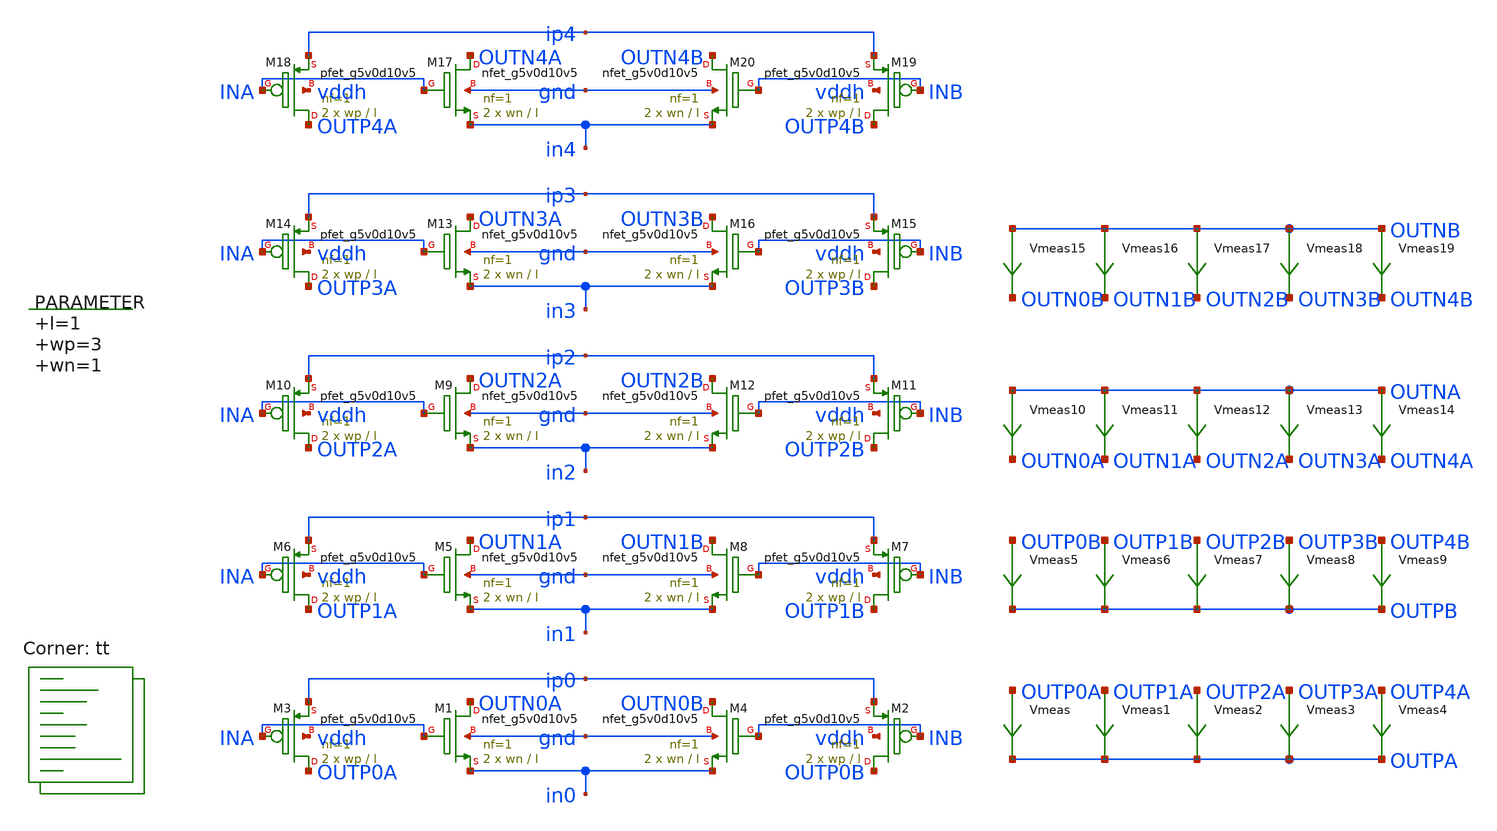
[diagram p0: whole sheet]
** sch_path: xschem/untitled.sch
**.subckt untitled
XM1 OUTN0A INA in0 gnd sky130_fd_pr__nfet_g5v0d10v5 L=l W=wn nf=1 ad='int((nf+1)/2) * W/nf * 0.29' as='int((nf+2)/2) * W/nf * 0.29'
+ pd='2*int((nf+1)/2) * (W/nf + 0.29)' ps='2*int((nf+2)/2) * (W/nf + 0.29)' nrd='0.29 / W' nrs='0.29 / W'
+ sa=0 sb=0 sd=0 mult=2 m=2
XM3 OUTP0A INA ip0 vddh sky130_fd_pr__pfet_g5v0d10v5 L=l W=wp nf=1 ad='int((nf+1)/2) * W/nf * 0.29' as='int((nf+2)/2) * W/nf * 0.29'
+ pd='2*int((nf+1)/2) * (W/nf + 0.29)' ps='2*int((nf+2)/2) * (W/nf + 0.29)' nrd='0.29 / W' nrs='0.29 / W'
+ sa=0 sb=0 sd=0 mult=2 m=2
XM2 OUTP0B INB ip0 vddh sky130_fd_pr__pfet_g5v0d10v5 L=l W=wp nf=1 ad='int((nf+1)/2) * W/nf * 0.29' as='int((nf+2)/2) * W/nf * 0.29'
+ pd='2*int((nf+1)/2) * (W/nf + 0.29)' ps='2*int((nf+2)/2) * (W/nf + 0.29)' nrd='0.29 / W' nrs='0.29 / W'
+ sa=0 sb=0 sd=0 mult=2 m=2
XM4 OUTN0B INB in0 gnd sky130_fd_pr__nfet_g5v0d10v5 L=l W=wn nf=1 ad='int((nf+1)/2) * W/nf * 0.29' as='int((nf+2)/2) * W/nf * 0.29'
+ pd='2*int((nf+1)/2) * (W/nf + 0.29)' ps='2*int((nf+2)/2) * (W/nf + 0.29)' nrd='0.29 / W' nrs='0.29 / W'
+ sa=0 sb=0 sd=0 mult=2 m=2
XM5 OUTN1A INA in1 gnd sky130_fd_pr__nfet_g5v0d10v5 L=l W=wn nf=1 ad='int((nf+1)/2) * W/nf * 0.29' as='int((nf+2)/2) * W/nf * 0.29'
+ pd='2*int((nf+1)/2) * (W/nf + 0.29)' ps='2*int((nf+2)/2) * (W/nf + 0.29)' nrd='0.29 / W' nrs='0.29 / W'
+ sa=0 sb=0 sd=0 mult=2 m=2
XM6 OUTP1A INA ip1 vddh sky130_fd_pr__pfet_g5v0d10v5 L=l W=wp nf=1 ad='int((nf+1)/2) * W/nf * 0.29' as='int((nf+2)/2) * W/nf * 0.29'
+ pd='2*int((nf+1)/2) * (W/nf + 0.29)' ps='2*int((nf+2)/2) * (W/nf + 0.29)' nrd='0.29 / W' nrs='0.29 / W'
+ sa=0 sb=0 sd=0 mult=2 m=2
XM7 OUTP1B INB ip1 vddh sky130_fd_pr__pfet_g5v0d10v5 L=l W=wp nf=1 ad='int((nf+1)/2) * W/nf * 0.29' as='int((nf+2)/2) * W/nf * 0.29'
+ pd='2*int((nf+1)/2) * (W/nf + 0.29)' ps='2*int((nf+2)/2) * (W/nf + 0.29)' nrd='0.29 / W' nrs='0.29 / W'
+ sa=0 sb=0 sd=0 mult=2 m=2
XM8 OUTN1B INB in1 gnd sky130_fd_pr__nfet_g5v0d10v5 L=l W=wn nf=1 ad='int((nf+1)/2) * W/nf * 0.29' as='int((nf+2)/2) * W/nf * 0.29'
+ pd='2*int((nf+1)/2) * (W/nf + 0.29)' ps='2*int((nf+2)/2) * (W/nf + 0.29)' nrd='0.29 / W' nrs='0.29 / W'
+ sa=0 sb=0 sd=0 mult=2 m=2
XM9 OUTN2A INA in2 gnd sky130_fd_pr__nfet_g5v0d10v5 L=l W=wn nf=1 ad='int((nf+1)/2) * W/nf * 0.29' as='int((nf+2)/2) * W/nf * 0.29'
+ pd='2*int((nf+1)/2) * (W/nf + 0.29)' ps='2*int((nf+2)/2) * (W/nf + 0.29)' nrd='0.29 / W' nrs='0.29 / W'
+ sa=0 sb=0 sd=0 mult=2 m=2
XM10 OUTP2A INA ip2 vddh sky130_fd_pr__pfet_g5v0d10v5 L=l W=wp nf=1 ad='int((nf+1)/2) * W/nf * 0.29'
+ as='int((nf+2)/2) * W/nf * 0.29' pd='2*int((nf+1)/2) * (W/nf + 0.29)' ps='2*int((nf+2)/2) * (W/nf + 0.29)'
+ nrd='0.29 / W' nrs='0.29 / W' sa=0 sb=0 sd=0 mult=2 m=2
XM11 OUTP2B INB ip2 vddh sky130_fd_pr__pfet_g5v0d10v5 L=l W=wp nf=1 ad='int((nf+1)/2) * W/nf * 0.29'
+ as='int((nf+2)/2) * W/nf * 0.29' pd='2*int((nf+1)/2) * (W/nf + 0.29)' ps='2*int((nf+2)/2) * (W/nf + 0.29)'
+ nrd='0.29 / W' nrs='0.29 / W' sa=0 sb=0 sd=0 mult=2 m=2
XM12 OUTN2B INB in2 gnd sky130_fd_pr__nfet_g5v0d10v5 L=l W=wn nf=1 ad='int((nf+1)/2) * W/nf * 0.29' as='int((nf+2)/2) * W/nf * 0.29'
+ pd='2*int((nf+1)/2) * (W/nf + 0.29)' ps='2*int((nf+2)/2) * (W/nf + 0.29)' nrd='0.29 / W' nrs='0.29 / W'
+ sa=0 sb=0 sd=0 mult=2 m=2
XM13 OUTN3A INA in3 gnd sky130_fd_pr__nfet_g5v0d10v5 L=l W=wn nf=1 ad='int((nf+1)/2) * W/nf * 0.29' as='int((nf+2)/2) * W/nf * 0.29'
+ pd='2*int((nf+1)/2) * (W/nf + 0.29)' ps='2*int((nf+2)/2) * (W/nf + 0.29)' nrd='0.29 / W' nrs='0.29 / W'
+ sa=0 sb=0 sd=0 mult=2 m=2
XM14 OUTP3A INA ip3 vddh sky130_fd_pr__pfet_g5v0d10v5 L=l W=wp nf=1 ad='int((nf+1)/2) * W/nf * 0.29'
+ as='int((nf+2)/2) * W/nf * 0.29' pd='2*int((nf+1)/2) * (W/nf + 0.29)' ps='2*int((nf+2)/2) * (W/nf + 0.29)'
+ nrd='0.29 / W' nrs='0.29 / W' sa=0 sb=0 sd=0 mult=2 m=2
XM15 OUTP3B INB ip3 vddh sky130_fd_pr__pfet_g5v0d10v5 L=l W=wp nf=1 ad='int((nf+1)/2) * W/nf * 0.29'
+ as='int((nf+2)/2) * W/nf * 0.29' pd='2*int((nf+1)/2) * (W/nf + 0.29)' ps='2*int((nf+2)/2) * (W/nf + 0.29)'
+ nrd='0.29 / W' nrs='0.29 / W' sa=0 sb=0 sd=0 mult=2 m=2
XM16 OUTN3B INB in3 gnd sky130_fd_pr__nfet_g5v0d10v5 L=l W=wn nf=1 ad='int((nf+1)/2) * W/nf * 0.29' as='int((nf+2)/2) * W/nf * 0.29'
+ pd='2*int((nf+1)/2) * (W/nf + 0.29)' ps='2*int((nf+2)/2) * (W/nf + 0.29)' nrd='0.29 / W' nrs='0.29 / W'
+ sa=0 sb=0 sd=0 mult=2 m=2
XM17 OUTN4A INA in4 gnd sky130_fd_pr__nfet_g5v0d10v5 L=l W=wn nf=1 ad='int((nf+1)/2) * W/nf * 0.29' as='int((nf+2)/2) * W/nf * 0.29'
+ pd='2*int((nf+1)/2) * (W/nf + 0.29)' ps='2*int((nf+2)/2) * (W/nf + 0.29)' nrd='0.29 / W' nrs='0.29 / W'
+ sa=0 sb=0 sd=0 mult=2 m=2
XM18 OUTP4A INA ip4 vddh sky130_fd_pr__pfet_g5v0d10v5 L=l W=wp nf=1 ad='int((nf+1)/2) * W/nf * 0.29'
+ as='int((nf+2)/2) * W/nf * 0.29' pd='2*int((nf+1)/2) * (W/nf + 0.29)' ps='2*int((nf+2)/2) * (W/nf + 0.29)'
+ nrd='0.29 / W' nrs='0.29 / W' sa=0 sb=0 sd=0 mult=2 m=2
XM19 OUTP4B INB ip4 vddh sky130_fd_pr__pfet_g5v0d10v5 L=l W=wp nf=1 ad='int((nf+1)/2) * W/nf * 0.29'
+ as='int((nf+2)/2) * W/nf * 0.29' pd='2*int((nf+1)/2) * (W/nf + 0.29)' ps='2*int((nf+2)/2) * (W/nf + 0.29)'
+ nrd='0.29 / W' nrs='0.29 / W' sa=0 sb=0 sd=0 mult=2 m=2
XM20 OUTN4B INB in4 gnd sky130_fd_pr__nfet_g5v0d10v5 L=l W=wn nf=1 ad='int((nf+1)/2) * W/nf * 0.29' as='int((nf+2)/2) * W/nf * 0.29'
+ pd='2*int((nf+1)/2) * (W/nf + 0.29)' ps='2*int((nf+2)/2) * (W/nf + 0.29)' nrd='0.29 / W' nrs='0.29 / W'
+ sa=0 sb=0 sd=0 mult=2 m=2
Vmeas OUTP0A OUTPA 0
.save i(vmeas)
Vmeas1 OUTP1A OUTPA 0
.save i(vmeas1)
Vmeas2 OUTP2A OUTPA 0
.save i(vmeas2)
Vmeas3 OUTP3A OUTPA 0
.save i(vmeas3)
Vmeas4 OUTP4A OUTPA 0
.save i(vmeas4)
Vmeas5 OUTP0B OUTPB 0
.save i(vmeas5)
Vmeas6 OUTP1B OUTPB 0
.save i(vmeas6)
Vmeas7 OUTP2B OUTPB 0
.save i(vmeas7)
Vmeas8 OUTP3B OUTPB 0
.save i(vmeas8)
Vmeas9 OUTP4B OUTPB 0
.save i(vmeas9)
Vmeas10 OUTNA OUTN0A 0
.save i(vmeas10)
Vmeas11 OUTNA OUTN1A 0
.save i(vmeas11)
Vmeas12 OUTNA OUTN2A 0
.save i(vmeas12)
Vmeas13 OUTNA OUTN3A 0
.save i(vmeas13)
Vmeas14 OUTNA OUTN4A 0
.save i(vmeas14)
Vmeas15 OUTNB OUTN0B 0
.save i(vmeas15)
Vmeas16 OUTNB OUTN1B 0
.save i(vmeas16)
Vmeas17 OUTNB OUTN2B 0
.save i(vmeas17)
Vmeas18 OUTNB OUTN3B 0
.save i(vmeas18)
Vmeas19 OUTNB OUTN4B 0
.save i(vmeas19)
.param l=1 wp=3 wn=1
**** begin user architecture code
.lib $::SKYWATER_MODELS/sky130.lib.spice tt



  .option wnflag=1
  .option safecurrents
  ********************Static Current Sources***************************
  .param base_current=1u
  .param i0=base_current i1={1*i0} i2={2*i0} i3={4*i0} i4={8*i0}
  Ip0 vddh ip0 i0
  In0 in0  gnd i0

  Ip1 vddh ip1 i1
  In1 in1  gnd i1

  Ip2 vddh ip2 i2
  In2 in2  gnd i2

  Ip3 vddh ip3 i3
  In3 in3  gnd i3

  Ip4 vddh ip4 i4
  In4 in4  gnd i4
  ********************Static Voltage Sources***************************
  Vddh vddh gnd dc 5.5

  vina ina gnd sin({5.5/2} {5.5/2} 100k)
  vinb inb gnd sin({5.5/2} {-5.5/2} 100k)
  ********************Dynamic Voltage Sources***************************
  *******Calculation**********
  .param base_f=100e3 base_t={1/base_f} base_th={base_t/2} base_d={base_th}
  .param d2_th ={base_th} d2_t={2*d2_th}
  .param d1_th ={4*d2_th} d1_t={d0_th}
  .param d0_th ={4*d1_th} d0_t={4*d0_th}

  .param d20_d ={0} d21_d={1*d2_th} d22_d={2*d2_th} d23_d={3*d2_th}
  .param d10_d ={0} d11_d={1*d1_th} d12_d={2*d1_th} d13_d={3*d1_th}
  .param d00_d ={0} d01_d={1*d0_th} d02_d={2*d0_th} d03_d={3*d0_th}
  *******Signals**********
  .param vhi=5.5
*  Vin1 b[0] gnd pulse(0 {vhi} {0} 1p 1p {10u} {20u})
*  Vin2 b[1] gnd pulse(0 {vhi} {0} 1p 1p {20u} {40u})
  ********************Simulation Commands*****************************
  .control
     reset
     save all
     tran 1n 30u
     *dc vin 0 5.5 0.001
     write input_stage-tb.raw
     set appendwrite
*    quit 0
  .endc



**** end user architecture code
**.ends
.end
